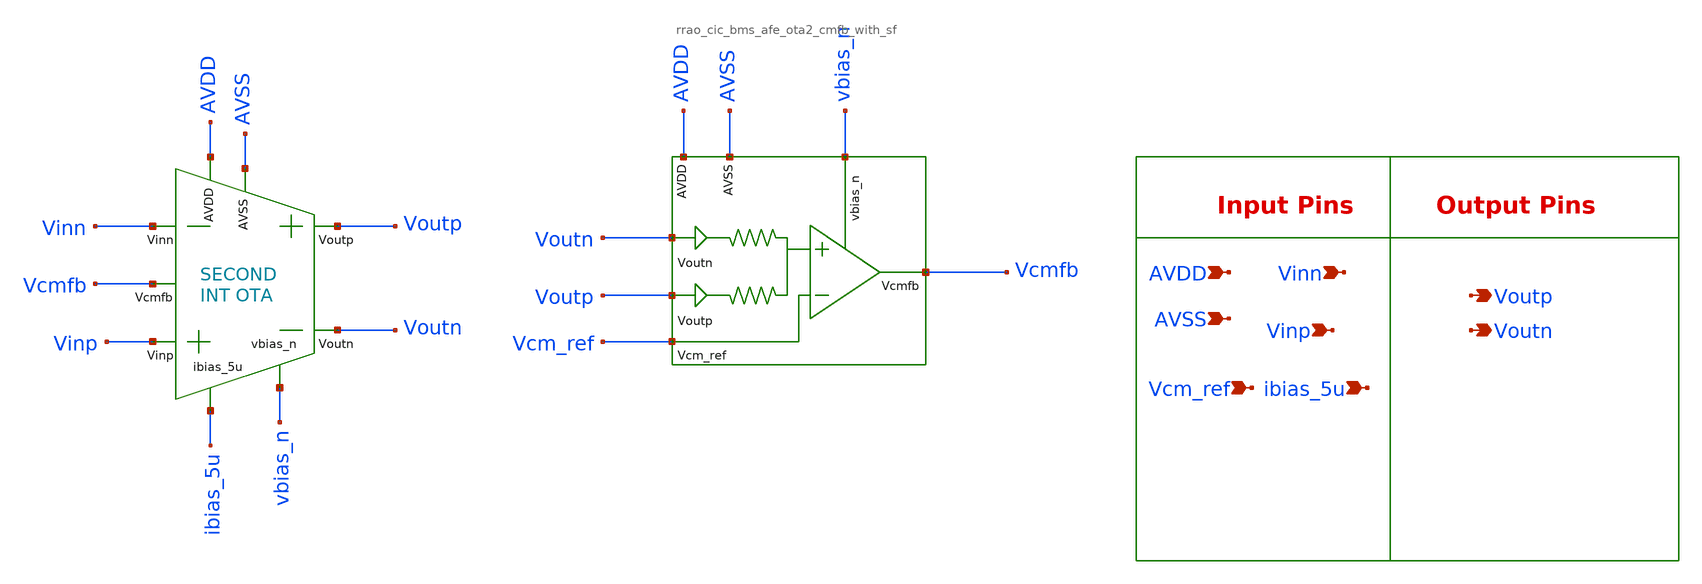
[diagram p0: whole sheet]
** sch_path: design/schematics/ADC/DSM_Loop_filter/Third_int/OTA_Files/rrao_cic_bms_afe_iadc_ota_with_cmfb.sch
**.subckt rrao_cic_bms_afe_iadc_ota_with_cmfb Vinp Vinn ibias_5u AVDD AVSS Voutp Voutn Vcm_ref
*.ipin Vinp
*.ipin Vinn
*.ipin ibias_5u
*.ipin AVDD
*.ipin AVSS
*.opin Voutp
*.opin Voutn
*.ipin Vcm_ref
x2 Vinp AVDD Voutp Vinn AVSS Voutn Vcmfb vbias_n ibias_5u rrao_cic_bms_afe_iadc_second_int_ota
x1 Vcmfb Vcm_ref AVDD Voutp vbias_n AVSS Voutn rrao_cic_bms_afe_ota2_cmfb_with_sf
**.ends
.end
